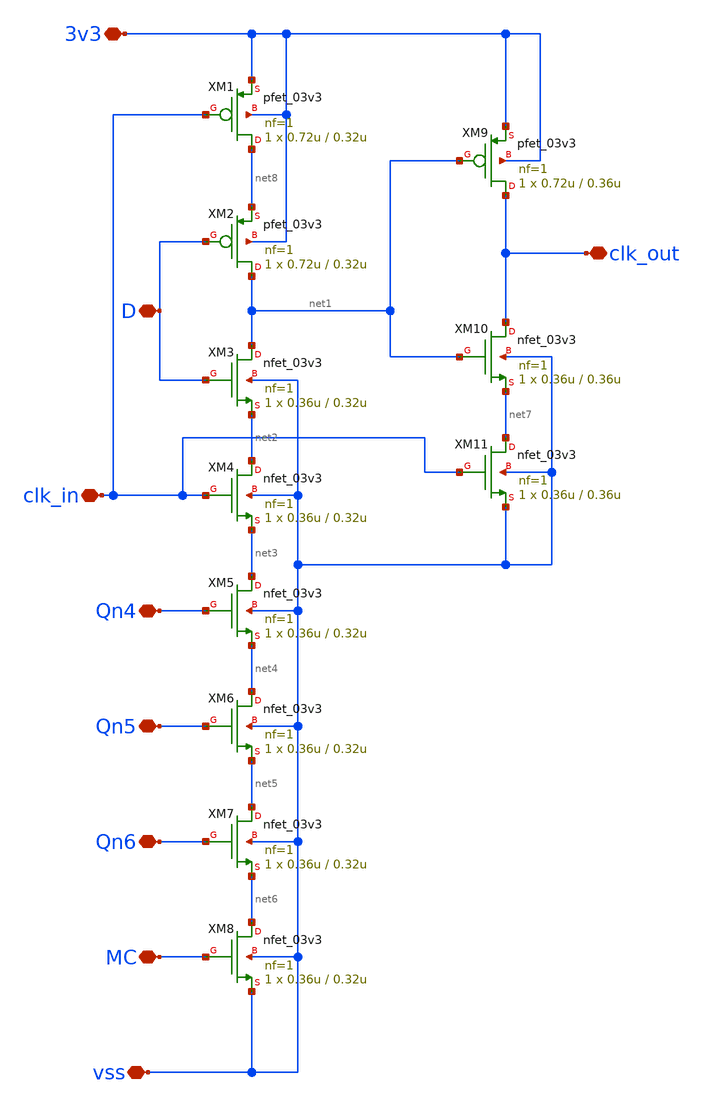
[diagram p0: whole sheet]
** sch_path: PLL/analog/schematics/Prescaler_FF1.sch
**.subckt Prescaler_FF1 D clk_in Qn4 Qn5 Qn6 vss 3v3 MC clk_out
*.iopin D
*.iopin clk_in
*.iopin Qn4
*.iopin Qn5
*.iopin Qn6
*.iopin vss
*.iopin 3v3
*.iopin MC
*.iopin clk_out
XM1 net8 clk_in 3v3 3v3 pfet_03v3 L=0.32u W=0.72u nf=1 ad='int((nf+1)/2) * W/nf * 0.18u' as='int((nf+2)/2) * W/nf * 0.18u'
+ pd='2*int((nf+1)/2) * (W/nf + 0.18u)' ps='2*int((nf+2)/2) * (W/nf + 0.18u)' nrd='0.18u / W' nrs='0.18u / W'
+ sa=0 sb=0 sd=0 m=1
XM2 net1 D net8 3v3 pfet_03v3 L=0.32u W=0.72u nf=1 ad='int((nf+1)/2) * W/nf * 0.18u' as='int((nf+2)/2) * W/nf * 0.18u'
+ pd='2*int((nf+1)/2) * (W/nf + 0.18u)' ps='2*int((nf+2)/2) * (W/nf + 0.18u)' nrd='0.18u / W' nrs='0.18u / W'
+ sa=0 sb=0 sd=0 m=1
XM3 net1 D net2 vss nfet_03v3 L=0.32u W=0.36u nf=1 ad='int((nf+1)/2) * W/nf * 0.18u' as='int((nf+2)/2) * W/nf * 0.18u'
+ pd='2*int((nf+1)/2) * (W/nf + 0.18u)' ps='2*int((nf+2)/2) * (W/nf + 0.18u)' nrd='0.18u / W' nrs='0.18u / W'
+ sa=0 sb=0 sd=0 m=1
XM4 net2 clk_in net3 vss nfet_03v3 L=0.32u W=0.36u nf=1 ad='int((nf+1)/2) * W/nf * 0.18u' as='int((nf+2)/2) * W/nf * 0.18u'
+ pd='2*int((nf+1)/2) * (W/nf + 0.18u)' ps='2*int((nf+2)/2) * (W/nf + 0.18u)' nrd='0.18u / W' nrs='0.18u / W'
+ sa=0 sb=0 sd=0 m=1
XM5 net3 Qn4 net4 vss nfet_03v3 L=0.32u W=0.36u nf=1 ad='int((nf+1)/2) * W/nf * 0.18u' as='int((nf+2)/2) * W/nf * 0.18u'
+ pd='2*int((nf+1)/2) * (W/nf + 0.18u)' ps='2*int((nf+2)/2) * (W/nf + 0.18u)' nrd='0.18u / W' nrs='0.18u / W'
+ sa=0 sb=0 sd=0 m=1
XM6 net4 Qn5 net5 vss nfet_03v3 L=0.32u W=0.36u nf=1 ad='int((nf+1)/2) * W/nf * 0.18u' as='int((nf+2)/2) * W/nf * 0.18u'
+ pd='2*int((nf+1)/2) * (W/nf + 0.18u)' ps='2*int((nf+2)/2) * (W/nf + 0.18u)' nrd='0.18u / W' nrs='0.18u / W'
+ sa=0 sb=0 sd=0 m=1
XM7 net5 Qn6 net6 vss nfet_03v3 L=0.32u W=0.36u nf=1 ad='int((nf+1)/2) * W/nf * 0.18u' as='int((nf+2)/2) * W/nf * 0.18u'
+ pd='2*int((nf+1)/2) * (W/nf + 0.18u)' ps='2*int((nf+2)/2) * (W/nf + 0.18u)' nrd='0.18u / W' nrs='0.18u / W'
+ sa=0 sb=0 sd=0 m=1
XM8 net6 MC vss vss nfet_03v3 L=0.32u W=0.36u nf=1 ad='int((nf+1)/2) * W/nf * 0.18u' as='int((nf+2)/2) * W/nf * 0.18u'
+ pd='2*int((nf+1)/2) * (W/nf + 0.18u)' ps='2*int((nf+2)/2) * (W/nf + 0.18u)' nrd='0.18u / W' nrs='0.18u / W'
+ sa=0 sb=0 sd=0 m=1
XM9 clk_out net1 3v3 3v3 pfet_03v3 L=0.36u W=0.72u nf=1 ad='int((nf+1)/2) * W/nf * 0.18u' as='int((nf+2)/2) * W/nf * 0.18u'
+ pd='2*int((nf+1)/2) * (W/nf + 0.18u)' ps='2*int((nf+2)/2) * (W/nf + 0.18u)' nrd='0.18u / W' nrs='0.18u / W'
+ sa=0 sb=0 sd=0 m=1
XM10 clk_out net1 net7 vss nfet_03v3 L=0.36u W=0.36u nf=1 ad='int((nf+1)/2) * W/nf * 0.18u' as='int((nf+2)/2) * W/nf * 0.18u'
+ pd='2*int((nf+1)/2) * (W/nf + 0.18u)' ps='2*int((nf+2)/2) * (W/nf + 0.18u)' nrd='0.18u / W' nrs='0.18u / W'
+ sa=0 sb=0 sd=0 m=1
XM11 net7 clk_in vss vss nfet_03v3 L=0.36u W=0.36u nf=1 ad='int((nf+1)/2) * W/nf * 0.18u' as='int((nf+2)/2) * W/nf * 0.18u'
+ pd='2*int((nf+1)/2) * (W/nf + 0.18u)' ps='2*int((nf+2)/2) * (W/nf + 0.18u)' nrd='0.18u / W' nrs='0.18u / W'
+ sa=0 sb=0 sd=0 m=1
**.ends
.end
